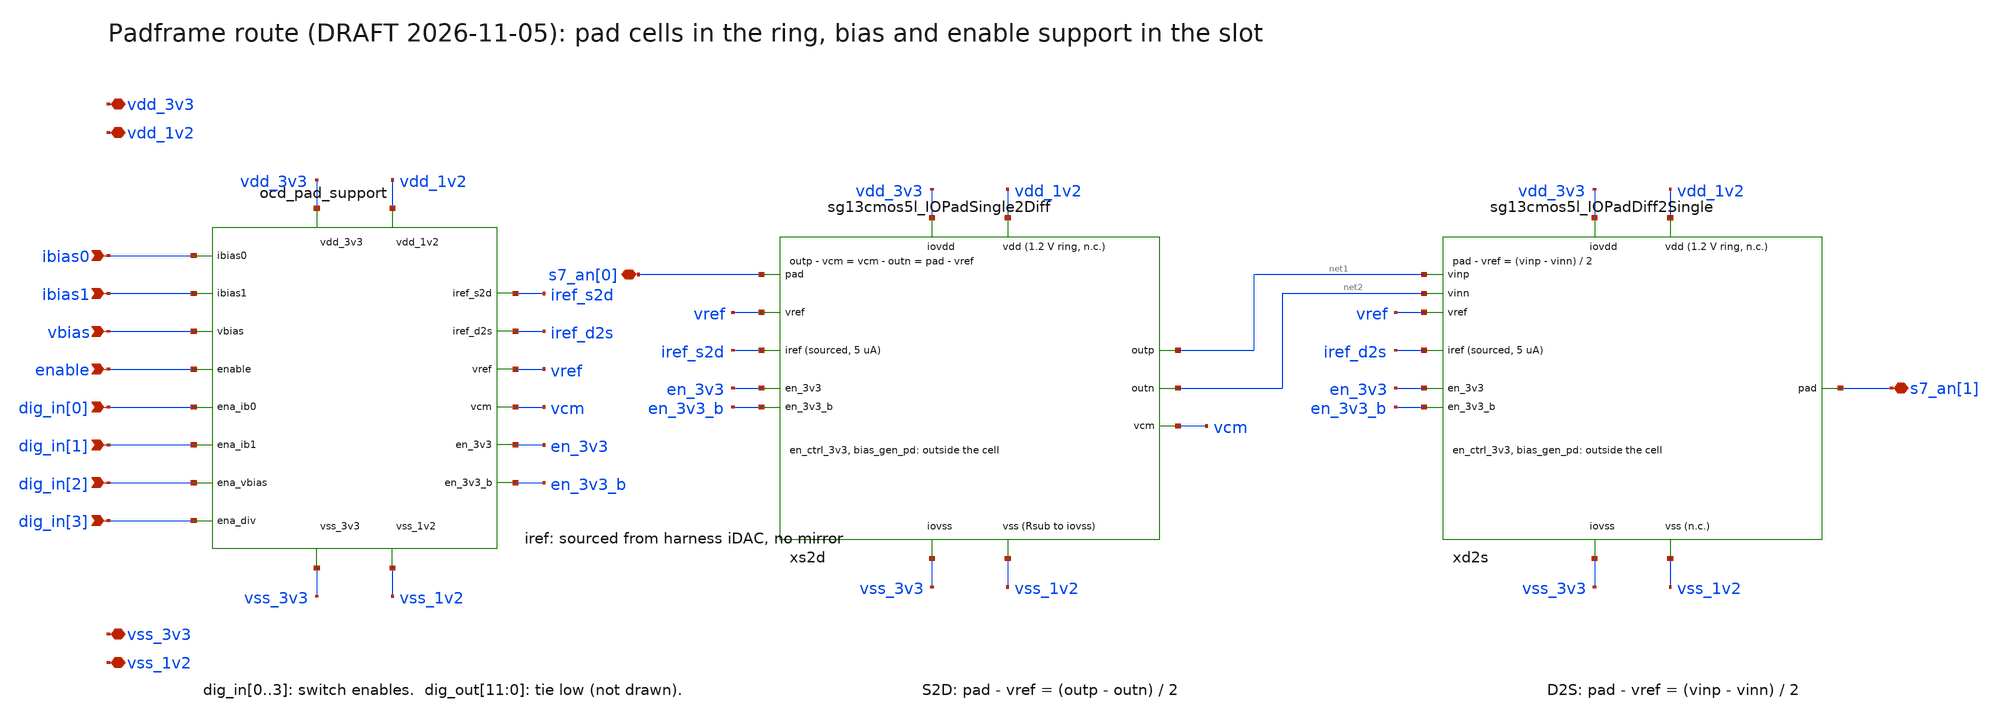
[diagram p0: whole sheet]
** sch_path: macros/ocd_pad_support/schematic/xschem/ocd_pad_route.sch
**.subckt ocd_pad_route ibias0 ibias1 vbias enable dig_in[0] dig_in[1] dig_in[2] dig_in[3] vdd_3v3
*+ vdd_1v2 vss_3v3 vss_1v2 s7_an[0] s7_an[1]
*.ipin ibias0
*.ipin ibias1
*.ipin vbias
*.ipin enable
*.ipin dig_in[0]
*.ipin dig_in[1]
*.ipin dig_in[2]
*.ipin dig_in[3]
*.iopin vdd_3v3
*.iopin vdd_1v2
*.iopin vss_3v3
*.iopin vss_1v2
*.iopin s7_an[0]
*.iopin s7_an[1]
xsup ibias0 ibias1 vbias enable dig_in[0] dig_in[1] dig_in[2] dig_in[3] vdd_1v2 vss_1v2 vdd_3v3
+ vss_3v3 iref_s2d iref_d2s en_3v3 en_3v3_b vref vcm ocd_pad_support
xs2d vdd_3v3 vss_3v3 vdd_1v2 vss_1v2 s7_an[0] net1 net2 vcm vref iref_s2d en_3v3 en_3v3_b
+ sg13cmos5l_IOPadSingle2Diff
xd2s vdd_3v3 vss_3v3 vdd_1v2 vss_1v2 s7_an[1] net1 net2 vref iref_d2s en_3v3 en_3v3_b
+ sg13cmos5l_IOPadDiff2Single
**.ends
.end
